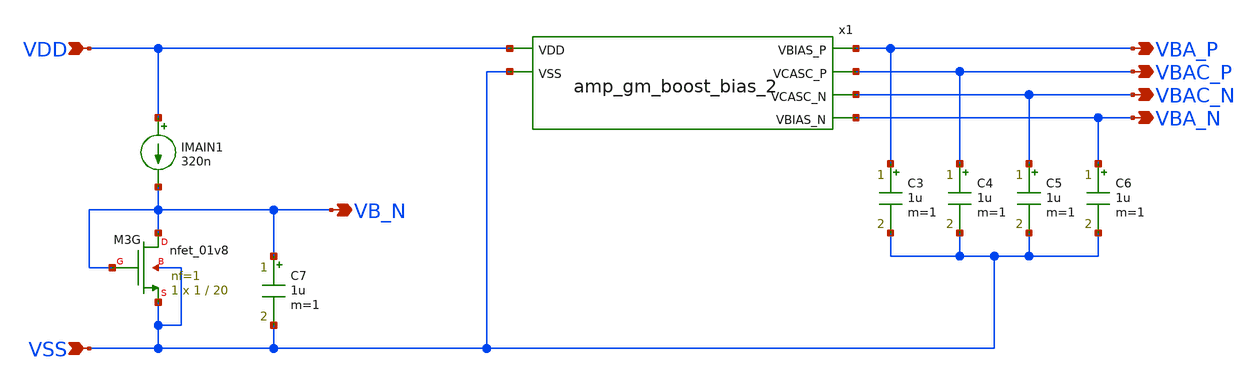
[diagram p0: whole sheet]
** sch_path: circuit-level/xschem/frontend/frontend_bias.sch
**.subckt frontend_bias VDD VSS VBA_P VBAC_P VBAC_N VBA_N VB_N
*.ipin VDD
*.ipin VSS
*.opin VBA_P
*.opin VBAC_P
*.opin VBAC_N
*.opin VBA_N
*.opin VB_N
XM3G VB_N VB_N VSS VSS sky130_fd_pr__nfet_01v8 L=20 W=1 nf=1 ad='int((nf+1)/2) * W/nf * 0.29' as='int((nf+2)/2) * W/nf * 0.29'
+ pd='2*int((nf+1)/2) * (W/nf + 0.29)' ps='2*int((nf+2)/2) * (W/nf + 0.29)' nrd='0.29 / W' nrs='0.29 / W'
+ sa=0 sb=0 sd=0 mult=1 m=1
IMAIN1 VDD VB_N 320n
C3 VBA_P VSS 1u m=1
C4 VBAC_P VSS 1u m=1
C5 VBAC_N VSS 1u m=1
C6 VBA_N VSS 1u m=1
C7 VB_N VSS 1u m=1
x1 VDD VBA_P VBAC_P VBAC_N VBA_N VSS amp_gm_boost_bias_2
**.ends

* expanding   symbol:  /foss/designs/aux-amp/amp_gm_boost_bias_2.sym # of pins=6
** sym_path: circuit-level/xschem/aux-amp/amp_gm_boost_bias_2.sym
** sch_path: circuit-level/xschem/aux-amp/amp_gm_boost_bias_2.sch
.subckt amp_gm_boost_bias_2 VDD VBIAS_P VCASC_P VCASC_N VBIAS_N VSS
*.opin VBIAS_P
*.ipin VSS
*.ipin VDD
*.opin VBIAS_N
*.opin VCASC_N
*.opin VCASC_P
XMn2 VBIAS_N VCASC_N net1 VSS sky130_fd_pr__nfet_01v8 L=1.5 W=2 nf=2 ad='int((nf+1)/2) * W/nf * 0.29'
+ as='int((nf+2)/2) * W/nf * 0.29' pd='2*int((nf+1)/2) * (W/nf + 0.29)' ps='2*int((nf+2)/2) * (W/nf + 0.29)'
+ nrd='0.29 / W' nrs='0.29 / W' sa=0 sb=0 sd=0 mult=1 m=1
XMn4 VCASC_N VCASC_N net2 VSS sky130_fd_pr__nfet_01v8 L=1.5 W=2 nf=2 ad='int((nf+1)/2) * W/nf * 0.29'
+ as='int((nf+2)/2) * W/nf * 0.29' pd='2*int((nf+1)/2) * (W/nf + 0.29)' ps='2*int((nf+2)/2) * (W/nf + 0.29)'
+ nrd='0.29 / W' nrs='0.29 / W' sa=0 sb=0 sd=0 mult=1 m=1
ICASCn VDD VCASC_N 150n
XMn1 net1 VBIAS_N VSS VSS sky130_fd_pr__nfet_01v8 L=80 W=8 nf=8 ad='int((nf+1)/2) * W/nf * 0.29' as='int((nf+2)/2) * W/nf * 0.29'
+ pd='2*int((nf+1)/2) * (W/nf + 0.29)' ps='2*int((nf+2)/2) * (W/nf + 0.29)' nrd='0.29 / W' nrs='0.29 / W'
+ sa=0 sb=0 sd=0 mult=1 m=1
IMAIN2 VBIAS_P VBIAS_N 50n
XMn3 net2 VCASC_N VSS VSS sky130_fd_pr__nfet_01v8 L=80 W=8 nf=8 ad='int((nf+1)/2) * W/nf * 0.29' as='int((nf+2)/2) * W/nf * 0.29'
+ pd='2*int((nf+1)/2) * (W/nf + 0.29)' ps='2*int((nf+2)/2) * (W/nf + 0.29)' nrd='0.29 / W' nrs='0.29 / W'
+ sa=0 sb=0 sd=0 mult=1 m=1
XMp1 VBIAS_P VBIAS_P VDD VDD sky130_fd_pr__pfet_01v8 L=10 W=1 nf=1 ad='int((nf+1)/2) * W/nf * 0.29' as='int((nf+2)/2) * W/nf * 0.29'
+ pd='2*int((nf+1)/2) * (W/nf + 0.29)' ps='2*int((nf+2)/2) * (W/nf + 0.29)' nrd='0.29 / W' nrs='0.29 / W'
+ sa=0 sb=0 sd=0 mult=1 m=1
ICASCp VCASC_P VSS 110n
XMp3 net3 VCASC_P VDD VDD sky130_fd_pr__pfet_01v8 L=80 W=10 nf=10 ad='int((nf+1)/2) * W/nf * 0.29' as='int((nf+2)/2) * W/nf * 0.29'
+ pd='2*int((nf+1)/2) * (W/nf + 0.29)' ps='2*int((nf+2)/2) * (W/nf + 0.29)' nrd='0.29 / W' nrs='0.29 / W'
+ sa=0 sb=0 sd=0 mult=1 m=1
XMp4 VCASC_P VCASC_P net3 VDD sky130_fd_pr__pfet_01v8 L=3.5 W=2 nf=2 ad='int((nf+1)/2) * W/nf * 0.29'
+ as='int((nf+2)/2) * W/nf * 0.29' pd='2*int((nf+1)/2) * (W/nf + 0.29)' ps='2*int((nf+2)/2) * (W/nf + 0.29)'
+ nrd='0.29 / W' nrs='0.29 / W' sa=0 sb=0 sd=0 mult=1 m=1
.ends

.end
